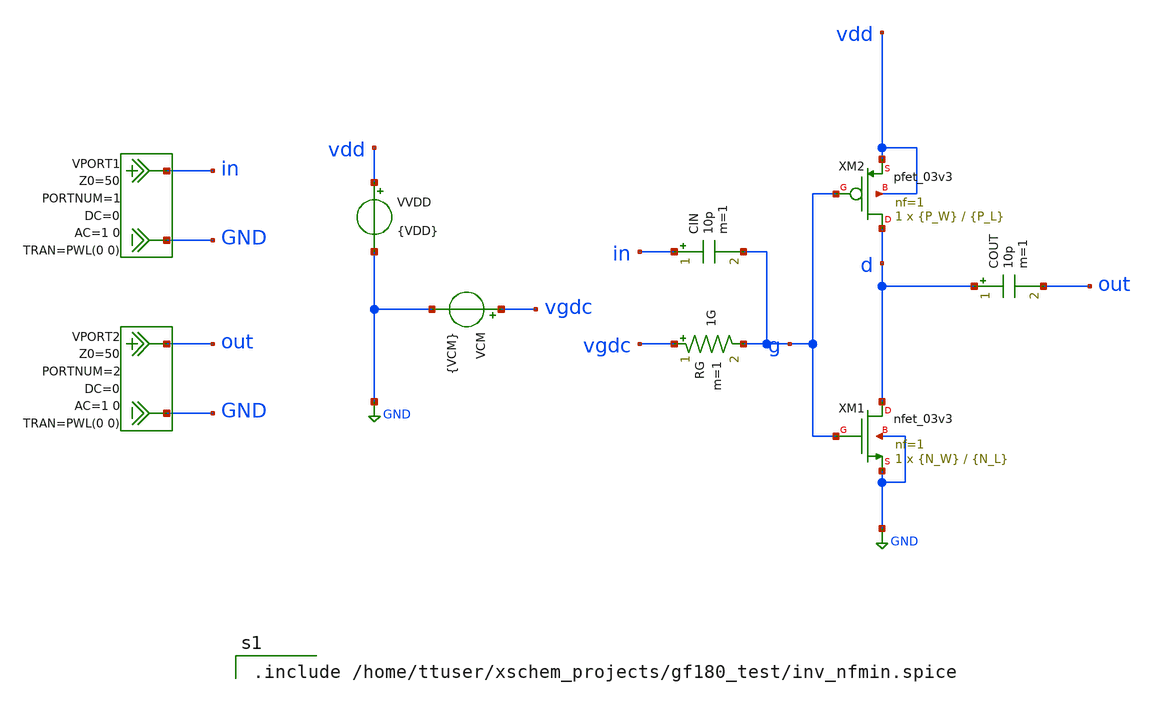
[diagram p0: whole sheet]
** sch_path: simulations/nfmin_sweeps/nfmin_jd_cmos_inv.sch
**.subckt nfmin_jd_cmos_inv
VCM vgdc GND {VCM}
VVDD vdd GND {VDD}
RG vgdc g 1G m=1
COUT d out 10p m=1
VPORT1 in GND DC 0 AC 1 0 portnum 1 z0 50 PWL(0 0)
VPORT2 out GND DC 0 AC 1 0 portnum 2 z0 50 PWL(0 0)
CIN in g 10p m=1
XM2 d g vdd vdd pfet_03v3 L={P_L} W={P_W} nf=1 ad='int((nf+1)/2) * W/nf * 0.18u' as='int((nf+2)/2) * W/nf * 0.18u'
+ pd='2*int((nf+1)/2) * (W/nf + 0.18u)' ps='2*int((nf+2)/2) * (W/nf + 0.18u)' nrd='0.18u / W' nrs='0.18u / W'
+ sa=0 sb=0 sd=0 m=1
XM1 d g GND GND nfet_03v3 L={N_L} W={N_W} nf=1 ad='int((nf+1)/2) * W/nf * 0.18u' as='int((nf+2)/2) * W/nf * 0.18u'
+ pd='2*int((nf+1)/2) * (W/nf + 0.18u)' ps='2*int((nf+2)/2) * (W/nf + 0.18u)' nrd='0.18u / W' nrs='0.18u / W'
+ sa=0 sb=0 sd=0 m=1
**** begin user architecture code

.include /home/ttuser/xschem_projects/gf180_test/inv_nfmin.spice

**** end user architecture code
**.ends
.GLOBAL GND
.end
